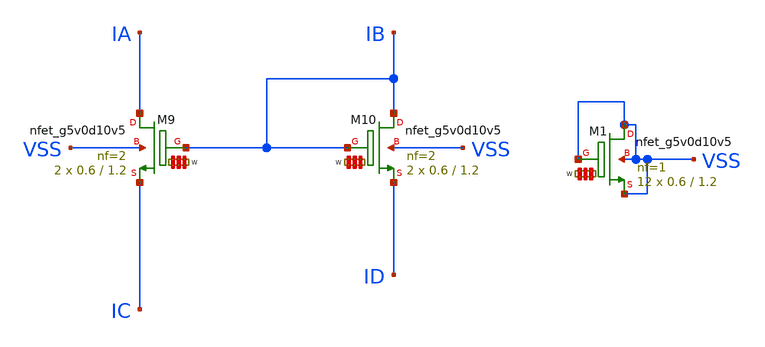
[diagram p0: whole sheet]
** sch_path: Learning/single_ended_amplifiers/Design_transcondutance_cell_sky130_5V/layout_example/upper_nmos_current_mirror/upper_nmos_current_mirror.sch
**.subckt upper_nmos_current_mirror
XM9 IA IB IC VSS sky130_fd_pr__nfet_g5v0d10v5 L=1.2 W='0.6 * 2 ' nf=2 ad='int((nf+1)/2) * W / nf * 0.29'
+ as='int((nf+2)/2) * W / nf * 0.29' pd='2*int((nf+1)/2) * (W / nf + 0.29)' ps='2*int((nf+2)/2) * (W / nf + 0.29)'
+ nrd='0.29 / W ' nrs='0.29 / W ' sa=0 sb=0 sd=0 mult=2 m=2
XM10 IB IB ID VSS sky130_fd_pr__nfet_g5v0d10v5 L=1.2 W='0.6 * 2 ' nf=2 ad='int((nf+1)/2) * W / nf * 0.29'
+ as='int((nf+2)/2) * W / nf * 0.29' pd='2*int((nf+1)/2) * (W / nf + 0.29)' ps='2*int((nf+2)/2) * (W / nf + 0.29)'
+ nrd='0.29 / W ' nrs='0.29 / W ' sa=0 sb=0 sd=0 mult=2 m=2
XM1 VSS VSS VSS VSS sky130_fd_pr__nfet_g5v0d10v5 L=1.2 W='0.6 * 1 ' nf=1 ad='int((nf+1)/2) * W / nf * 0.29'
+ as='int((nf+2)/2) * W / nf * 0.29' pd='2*int((nf+1)/2) * (W / nf + 0.29)' ps='2*int((nf+2)/2) * (W / nf + 0.29)'
+ nrd='0.29 / W ' nrs='0.29 / W ' sa=0 sb=0 sd=0 mult=12 m=12
**.ends
.end
